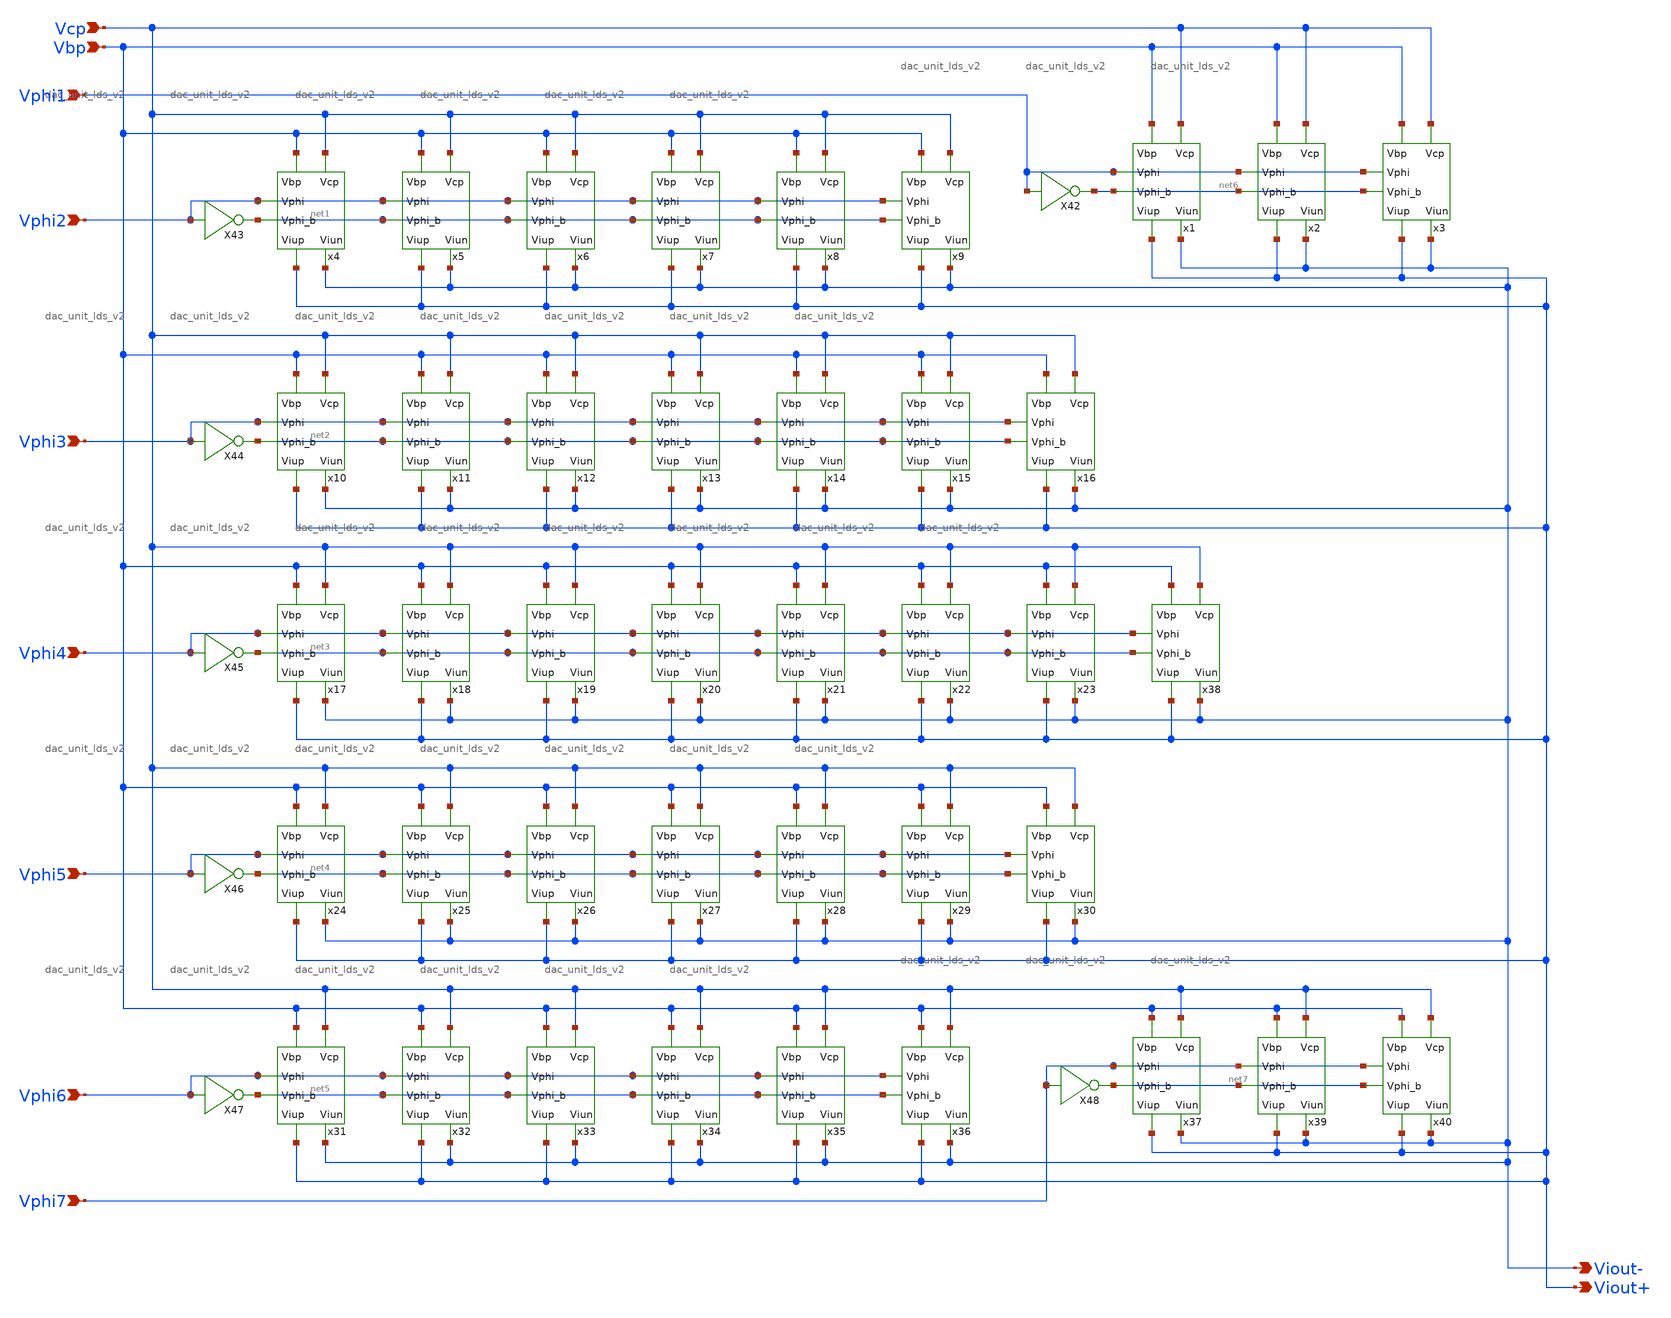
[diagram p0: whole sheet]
** sch_path: simulation/archived/dac_lds_2.sch
**.subckt dac_lds_2 Vphi1 Vphi2 Vphi3 Vphi4 Vphi5 Vphi6 Vphi7 Viout+ Viout- Vcp Vbp
*.ipin Vphi1
*.ipin Vphi2
*.ipin Vphi3
*.ipin Vphi4
*.ipin Vphi5
*.ipin Vphi6
*.ipin Vphi7
*.opin Viout+
*.opin Viout-
*.ipin Vcp
*.ipin Vbp
x1 Vbp Vcp Viout+ Viout- Vphi1 net6 dac_unit_lds_v2
x2 Vbp Vcp Viout+ Viout- Vphi1 net6 dac_unit_lds_v2
x3 Vbp Vcp Viout+ Viout- Vphi1 net6 dac_unit_lds_v2
x4 Vbp Vcp Viout+ Viout- Vphi2 net1 dac_unit_lds_v2
x5 Vbp Vcp Viout+ Viout- Vphi2 net1 dac_unit_lds_v2
x6 Vbp Vcp Viout+ Viout- Vphi2 net1 dac_unit_lds_v2
x7 Vbp Vcp Viout+ Viout- Vphi2 net1 dac_unit_lds_v2
x8 Vbp Vcp Viout+ Viout- Vphi2 net1 dac_unit_lds_v2
x9 Vbp Vcp Viout+ Viout- Vphi2 net1 dac_unit_lds_v2
x10 Vbp Vcp Viout+ Viout- Vphi3 net2 dac_unit_lds_v2
x11 Vbp Vcp Viout+ Viout- Vphi3 net2 dac_unit_lds_v2
x12 Vbp Vcp Viout+ Viout- Vphi3 net2 dac_unit_lds_v2
x13 Vbp Vcp Viout+ Viout- Vphi3 net2 dac_unit_lds_v2
x14 Vbp Vcp Viout+ Viout- Vphi3 net2 dac_unit_lds_v2
x15 Vbp Vcp Viout+ Viout- Vphi3 net2 dac_unit_lds_v2
x16 Vbp Vcp Viout+ Viout- Vphi3 net2 dac_unit_lds_v2
x17 Vbp Vcp Viout+ Viout- Vphi4 net3 dac_unit_lds_v2
x18 Vbp Vcp Viout+ Viout- Vphi4 net3 dac_unit_lds_v2
x19 Vbp Vcp Viout+ Viout- Vphi4 net3 dac_unit_lds_v2
x20 Vbp Vcp Viout+ Viout- Vphi4 net3 dac_unit_lds_v2
x21 Vbp Vcp Viout+ Viout- Vphi4 net3 dac_unit_lds_v2
x22 Vbp Vcp Viout+ Viout- Vphi4 net3 dac_unit_lds_v2
x23 Vbp Vcp Viout+ Viout- Vphi4 net3 dac_unit_lds_v2
x24 Vbp Vcp Viout+ Viout- Vphi5 net4 dac_unit_lds_v2
x25 Vbp Vcp Viout+ Viout- Vphi5 net4 dac_unit_lds_v2
x26 Vbp Vcp Viout+ Viout- Vphi5 net4 dac_unit_lds_v2
x27 Vbp Vcp Viout+ Viout- Vphi5 net4 dac_unit_lds_v2
x28 Vbp Vcp Viout+ Viout- Vphi5 net4 dac_unit_lds_v2
x29 Vbp Vcp Viout+ Viout- Vphi5 net4 dac_unit_lds_v2
x30 Vbp Vcp Viout+ Viout- Vphi5 net4 dac_unit_lds_v2
x31 Vbp Vcp Viout+ Viout- Vphi6 net5 dac_unit_lds_v2
x32 Vbp Vcp Viout+ Viout- Vphi6 net5 dac_unit_lds_v2
x33 Vbp Vcp Viout+ Viout- Vphi6 net5 dac_unit_lds_v2
x34 Vbp Vcp Viout+ Viout- Vphi6 net5 dac_unit_lds_v2
x35 Vbp Vcp Viout+ Viout- Vphi6 net5 dac_unit_lds_v2
x36 Vbp Vcp Viout+ Viout- Vphi6 net5 dac_unit_lds_v2
x38 Vbp Vcp Viout+ Viout- Vphi4 net3 dac_unit_lds_v2
x37 Vbp Vcp Viout+ Viout- Vphi7 net7 dac_unit_lds_v2
x39 Vbp Vcp Viout+ Viout- Vphi7 net7 dac_unit_lds_v2
x40 Vbp Vcp Viout+ Viout- Vphi7 net7 dac_unit_lds_v2
X42 Vphi1 net6 inverter
X43 Vphi2 net1 inverter
X44 Vphi3 net2 inverter
X45 Vphi4 net3 inverter
X46 Vphi5 net4 inverter
X47 Vphi6 net5 inverter
X48 Vphi7 net7 inverter
**.ends

* expanding   symbol:  ./dac/dac_unit_lds_v2.sym # of pins=6
** sym_path: simulation/dac/dac_unit_lds_v2.sym
** sch_path: simulation/dac/dac_unit_lds_v2.sch
.subckt dac_unit_lds_v2 Vbp Vcp Viup Viun Vphi Vphi_b
*.ipin Vphi
*.ipin Vbp
*.ipin Vcp
*.opin Viun
*.opin Viup
*.ipin Vphi_b
XM1 net1 Vbp VDD VDD sky130_fd_pr__pfet_01v8 L=0.5 W=6 nf=1 ad='int((nf+1)/2) * W/nf * 0.29' as='int((nf+2)/2) * W/nf * 0.29'
+ pd='2*int((nf+1)/2) * (W/nf + 0.29)' ps='2*int((nf+2)/2) * (W/nf + 0.29)' nrd='0.29 / W' nrs='0.29 / W'
+ sa=0 sb=0 sd=0 mult=1 m=1
XM2 net2 Vcp net1 VDD sky130_fd_pr__pfet_01v8 L=0.5 W=6 nf=1 ad='int((nf+1)/2) * W/nf * 0.29' as='int((nf+2)/2) * W/nf * 0.29'
+ pd='2*int((nf+1)/2) * (W/nf + 0.29)' ps='2*int((nf+2)/2) * (W/nf + 0.29)' nrd='0.29 / W' nrs='0.29 / W'
+ sa=0 sb=0 sd=0 mult=1 m=1
XM3 Viun Vphi net2 VDD sky130_fd_pr__pfet_01v8 L=0.5 W=6 nf=1 ad='int((nf+1)/2) * W/nf * 0.29' as='int((nf+2)/2) * W/nf * 0.29'
+ pd='2*int((nf+1)/2) * (W/nf + 0.29)' ps='2*int((nf+2)/2) * (W/nf + 0.29)' nrd='0.29 / W' nrs='0.29 / W'
+ sa=0 sb=0 sd=0 mult=1 m=1
XM4 Viup Vphi_b net2 VDD sky130_fd_pr__pfet_01v8 L=0.5 W=6 nf=1 ad='int((nf+1)/2) * W/nf * 0.29' as='int((nf+2)/2) * W/nf * 0.29'
+ pd='2*int((nf+1)/2) * (W/nf + 0.29)' ps='2*int((nf+2)/2) * (W/nf + 0.29)' nrd='0.29 / W' nrs='0.29 / W'
+ sa=0 sb=0 sd=0 mult=1 m=1
XM5 net3 Vbp VDD VDD sky130_fd_pr__pfet_01v8 L=0.5 W=6 nf=1 ad='int((nf+1)/2) * W/nf * 0.29' as='int((nf+2)/2) * W/nf * 0.29'
+ pd='2*int((nf+1)/2) * (W/nf + 0.29)' ps='2*int((nf+2)/2) * (W/nf + 0.29)' nrd='0.29 / W' nrs='0.29 / W'
+ sa=0 sb=0 sd=0 mult=1 m=1
XM6 net4 Vcp net3 VDD sky130_fd_pr__pfet_01v8 L=0.5 W=6 nf=1 ad='int((nf+1)/2) * W/nf * 0.29' as='int((nf+2)/2) * W/nf * 0.29'
+ pd='2*int((nf+1)/2) * (W/nf + 0.29)' ps='2*int((nf+2)/2) * (W/nf + 0.29)' nrd='0.29 / W' nrs='0.29 / W'
+ sa=0 sb=0 sd=0 mult=1 m=1
XM7 Viun Vphi net4 VDD sky130_fd_pr__pfet_01v8 L=0.5 W=6 nf=1 ad='int((nf+1)/2) * W/nf * 0.29' as='int((nf+2)/2) * W/nf * 0.29'
+ pd='2*int((nf+1)/2) * (W/nf + 0.29)' ps='2*int((nf+2)/2) * (W/nf + 0.29)' nrd='0.29 / W' nrs='0.29 / W'
+ sa=0 sb=0 sd=0 mult=1 m=1
XM8 Viup Vphi_b net4 VDD sky130_fd_pr__pfet_01v8 L=0.5 W=6 nf=1 ad='int((nf+1)/2) * W/nf * 0.29' as='int((nf+2)/2) * W/nf * 0.29'
+ pd='2*int((nf+1)/2) * (W/nf + 0.29)' ps='2*int((nf+2)/2) * (W/nf + 0.29)' nrd='0.29 / W' nrs='0.29 / W'
+ sa=0 sb=0 sd=0 mult=1 m=1
XM9 VDD VDD net1 VDD sky130_fd_pr__pfet_01v8 L=0.5 W=6 nf=1 ad='int((nf+1)/2) * W/nf * 0.29' as='int((nf+2)/2) * W/nf * 0.29'
+ pd='2*int((nf+1)/2) * (W/nf + 0.29)' ps='2*int((nf+2)/2) * (W/nf + 0.29)' nrd='0.29 / W' nrs='0.29 / W'
+ sa=0 sb=0 sd=0 mult=1 m=1
XM10 net1 VDD VDD VDD sky130_fd_pr__pfet_01v8 L=0.5 W=6 nf=1 ad='int((nf+1)/2) * W/nf * 0.29' as='int((nf+2)/2) * W/nf * 0.29'
+ pd='2*int((nf+1)/2) * (W/nf + 0.29)' ps='2*int((nf+2)/2) * (W/nf + 0.29)' nrd='0.29 / W' nrs='0.29 / W'
+ sa=0 sb=0 sd=0 mult=1 m=1
XM11 VDD VDD net3 VDD sky130_fd_pr__pfet_01v8 L=0.5 W=6 nf=1 ad='int((nf+1)/2) * W/nf * 0.29' as='int((nf+2)/2) * W/nf * 0.29'
+ pd='2*int((nf+1)/2) * (W/nf + 0.29)' ps='2*int((nf+2)/2) * (W/nf + 0.29)' nrd='0.29 / W' nrs='0.29 / W'
+ sa=0 sb=0 sd=0 mult=1 m=1
XM12 net3 VDD VDD VDD sky130_fd_pr__pfet_01v8 L=0.5 W=6 nf=1 ad='int((nf+1)/2) * W/nf * 0.29' as='int((nf+2)/2) * W/nf * 0.29'
+ pd='2*int((nf+1)/2) * (W/nf + 0.29)' ps='2*int((nf+2)/2) * (W/nf + 0.29)' nrd='0.29 / W' nrs='0.29 / W'
+ sa=0 sb=0 sd=0 mult=1 m=1
.ends


* expanding   symbol:  ./dac/inverter.sym # of pins=2
** sym_path: simulation/dac/inverter.sym
** sch_path: simulation/dac/inverter.sch
.subckt inverter A Y
*.ipin A
*.opin Y
XM1 Y A VDD VDD sky130_fd_pr__pfet_01v8 L=0.15 W=1 nf=1 ad='int((nf+1)/2) * W/nf * 0.29' as='int((nf+2)/2) * W/nf * 0.29'
+ pd='2*int((nf+1)/2) * (W/nf + 0.29)' ps='2*int((nf+2)/2) * (W/nf + 0.29)' nrd='0.29 / W' nrs='0.29 / W'
+ sa=0 sb=0 sd=0 mult=1 m=1
XM2 Y A GND GND sky130_fd_pr__nfet_01v8 L=0.15 W=1 nf=1 ad='int((nf+1)/2) * W/nf * 0.29' as='int((nf+2)/2) * W/nf * 0.29'
+ pd='2*int((nf+1)/2) * (W/nf + 0.29)' ps='2*int((nf+2)/2) * (W/nf + 0.29)' nrd='0.29 / W' nrs='0.29 / W'
+ sa=0 sb=0 sd=0 mult=1 m=1
.ends

.GLOBAL VDD
.GLOBAL GND
.end
